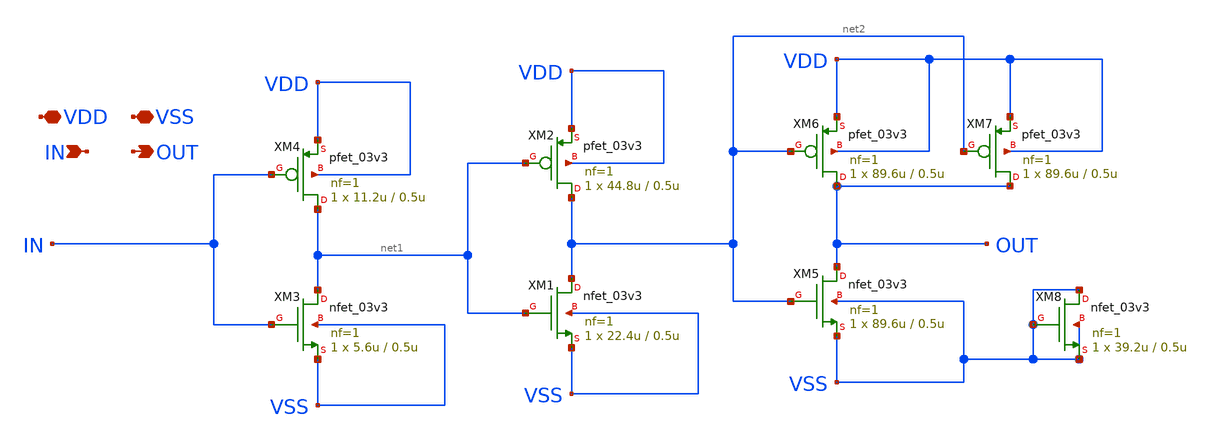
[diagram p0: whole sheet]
** sch_path: PLL-main/schematic/xschem/Tappered-Buffer_1.sch
**.subckt Tappered-Buffer_1 VDD VSS IN OUT
*.iopin VDD
*.iopin VSS
*.ipin IN
*.opin OUT
XM3 net1 IN VSS VSS nfet_03v3 L=0.5u W=5.6u nf=1 ad='int((nf+1)/2) * W/nf * 0.18u' as='int((nf+2)/2) * W/nf * 0.18u'
+ pd='2*int((nf+1)/2) * (W/nf + 0.18u)' ps='2*int((nf+2)/2) * (W/nf + 0.18u)' nrd='0.18u / W' nrs='0.18u / W'
+ sa=0 sb=0 sd=0 m=1
XM4 net1 IN VDD VDD pfet_03v3 L=0.5u W=11.2u nf=1 ad='int((nf+1)/2) * W/nf * 0.18u' as='int((nf+2)/2) * W/nf * 0.18u'
+ pd='2*int((nf+1)/2) * (W/nf + 0.18u)' ps='2*int((nf+2)/2) * (W/nf + 0.18u)' nrd='0.18u / W' nrs='0.18u / W'
+ sa=0 sb=0 sd=0 m=1
XM1 net2 net1 VSS VSS nfet_03v3 L=0.5u W=22.4u nf=1 ad='int((nf+1)/2) * W/nf * 0.18u' as='int((nf+2)/2) * W/nf * 0.18u'
+ pd='2*int((nf+1)/2) * (W/nf + 0.18u)' ps='2*int((nf+2)/2) * (W/nf + 0.18u)' nrd='0.18u / W' nrs='0.18u / W'
+ sa=0 sb=0 sd=0 m=1
XM2 net2 net1 VDD VDD pfet_03v3 L=0.5u W=44.8u nf=1 ad='int((nf+1)/2) * W/nf * 0.18u' as='int((nf+2)/2) * W/nf * 0.18u'
+ pd='2*int((nf+1)/2) * (W/nf + 0.18u)' ps='2*int((nf+2)/2) * (W/nf + 0.18u)' nrd='0.18u / W' nrs='0.18u / W'
+ sa=0 sb=0 sd=0 m=1
XM5 OUT net2 VSS VSS nfet_03v3 L=0.5u W=89.6u nf=1 ad='int((nf+1)/2) * W/nf * 0.18u' as='int((nf+2)/2) * W/nf * 0.18u'
+ pd='2*int((nf+1)/2) * (W/nf + 0.18u)' ps='2*int((nf+2)/2) * (W/nf + 0.18u)' nrd='0.18u / W' nrs='0.18u / W'
+ sa=0 sb=0 sd=0 m=1
XM6 OUT net2 VDD VDD pfet_03v3 L=0.5u W=89.6u nf=1 ad='int((nf+1)/2) * W/nf * 0.18u' as='int((nf+2)/2) * W/nf * 0.18u'
+ pd='2*int((nf+1)/2) * (W/nf + 0.18u)' ps='2*int((nf+2)/2) * (W/nf + 0.18u)' nrd='0.18u / W' nrs='0.18u / W'
+ sa=0 sb=0 sd=0 m=1
XM7 OUT net2 VDD VDD pfet_03v3 L=0.5u W=89.6u nf=1 ad='int((nf+1)/2) * W/nf * 0.18u' as='int((nf+2)/2) * W/nf * 0.18u'
+ pd='2*int((nf+1)/2) * (W/nf + 0.18u)' ps='2*int((nf+2)/2) * (W/nf + 0.18u)' nrd='0.18u / W' nrs='0.18u / W'
+ sa=0 sb=0 sd=0 m=1
XM8 VSS VSS VSS VSS nfet_03v3 L=0.5u W=39.2u nf=1 ad='int((nf+1)/2) * W/nf * 0.18u' as='int((nf+2)/2) * W/nf * 0.18u'
+ pd='2*int((nf+1)/2) * (W/nf + 0.18u)' ps='2*int((nf+2)/2) * (W/nf + 0.18u)' nrd='0.18u / W' nrs='0.18u / W'
+ sa=0 sb=0 sd=0 m=1
**.ends
.end
